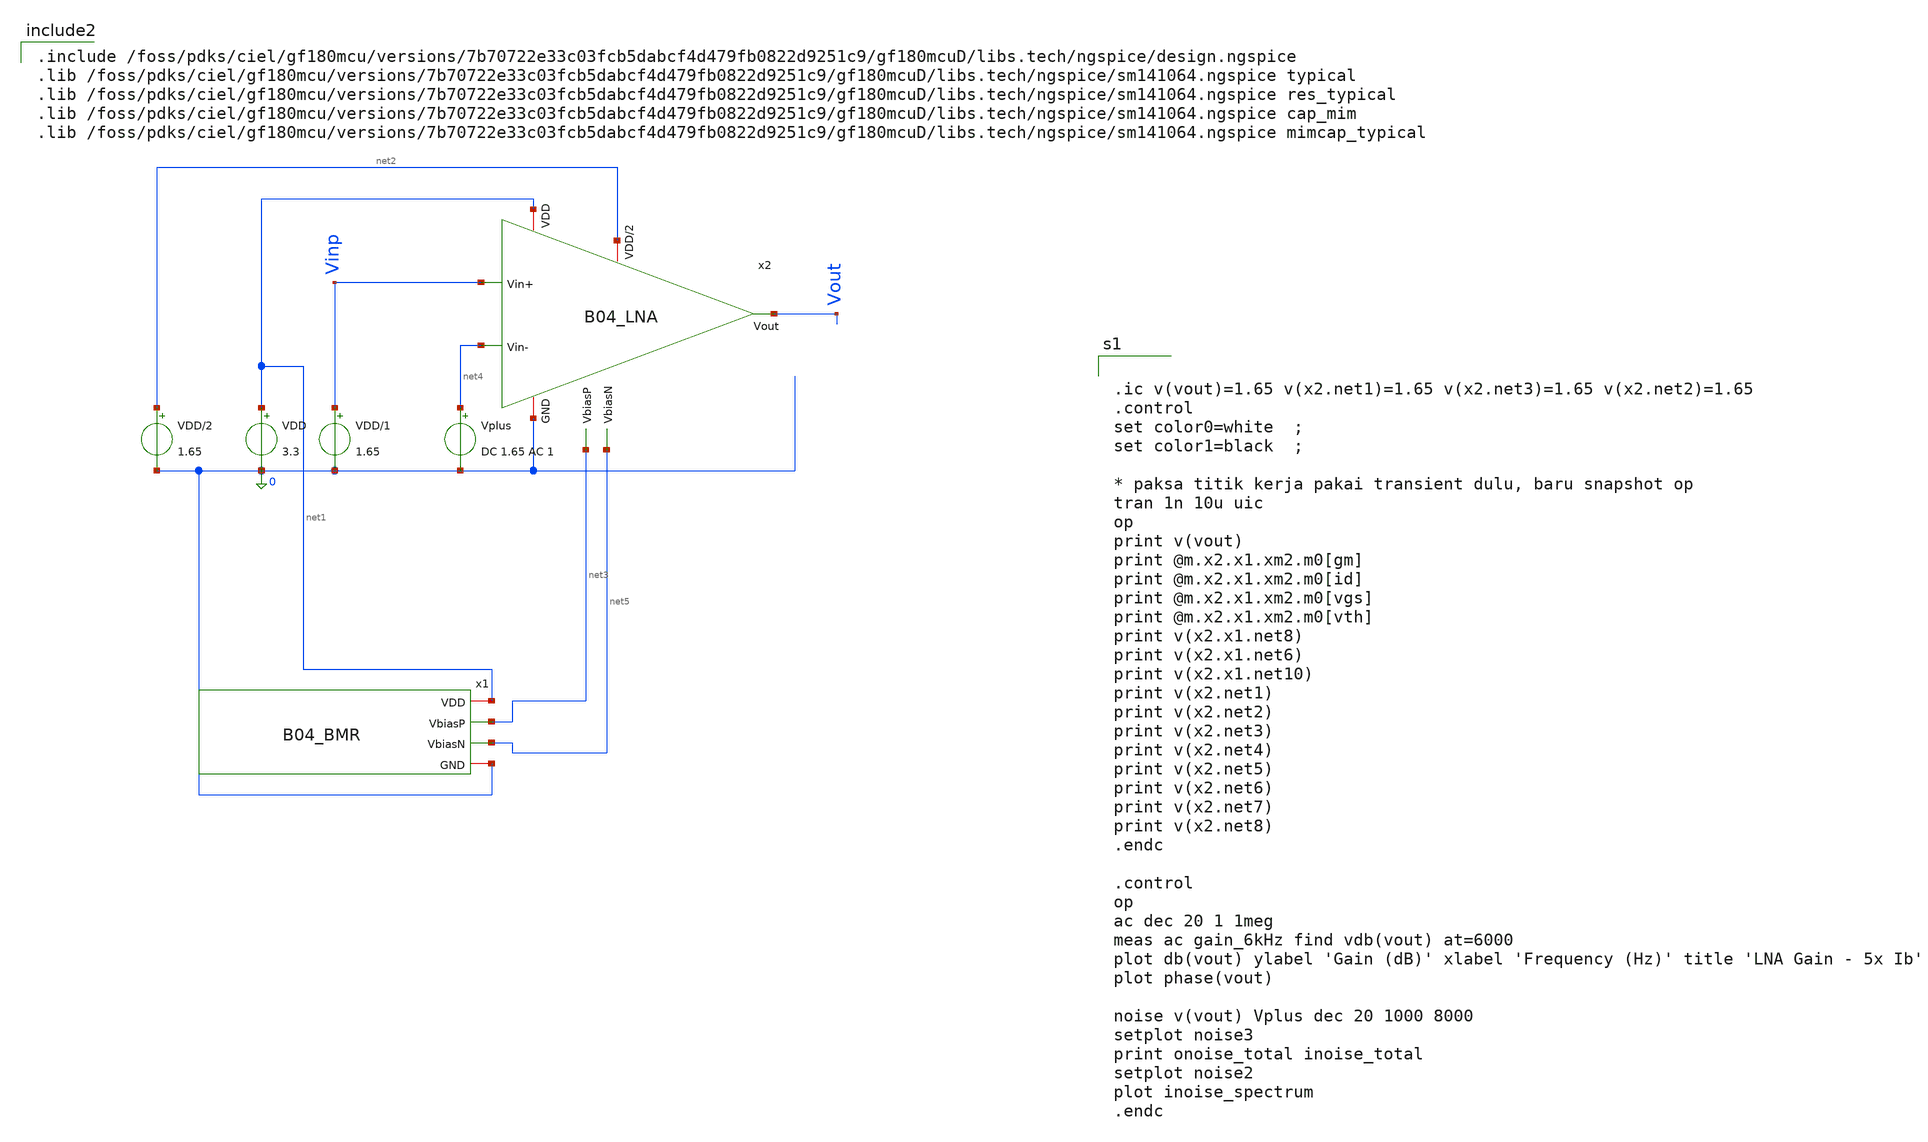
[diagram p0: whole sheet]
** sch_path: analog/B04_tb_LNA.sch
**.subckt B04_tb_LNA
VDD net1 0 3.3
Vplus net4 0 DC 1.65 AC 1
x2 net1 net2 Vinp Vout net4 0 net3 net5 B04_LNA
VDD/2 net2 0 1.65
VDD/1 Vinp 0 1.65
x1 net1 net3 net5 0 B04_BMR
**** begin user architecture code


.ic v(vout)=1.65 v(x2.net1)=1.65 v(x2.net3)=1.65 v(x2.net2)=1.65
.control
set color0=white  ;
set color1=black  ;

* paksa titik kerja pakai transient dulu, baru snapshot op
tran 1n 10u uic
op
print v(vout)
print @m.x2.x1.xm2.m0[gm]
print @m.x2.x1.xm2.m0[id]
print @m.x2.x1.xm2.m0[vgs]
print @m.x2.x1.xm2.m0[vth]
print v(x2.x1.net8)
print v(x2.x1.net6)
print v(x2.x1.net10)
print v(x2.net1)
print v(x2.net2)
print v(x2.net3)
print v(x2.net4)
print v(x2.net5)
print v(x2.net6)
print v(x2.net7)
print v(x2.net8)
.endc

.control
op
ac dec 20 1 1meg
meas ac gain_6kHz find vdb(vout) at=6000
plot db(vout) ylabel 'Gain (dB)' xlabel 'Frequency (Hz)' title 'LNA Gain - 5x Ib'
plot phase(vout)

noise v(vout) Vplus dec 20 1000 8000
setplot noise3
print onoise_total inoise_total
setplot noise2
plot inoise_spectrum
.endc



.include /foss/pdks/ciel/gf180mcu/versions/7b70722e33c03fcb5dabcf4d479fb0822d9251c9/gf180mcuD/libs.tech/ngspice/design.ngspice
.lib /foss/pdks/ciel/gf180mcu/versions/7b70722e33c03fcb5dabcf4d479fb0822d9251c9/gf180mcuD/libs.tech/ngspice/sm141064.ngspice typical
.lib /foss/pdks/ciel/gf180mcu/versions/7b70722e33c03fcb5dabcf4d479fb0822d9251c9/gf180mcuD/libs.tech/ngspice/sm141064.ngspice res_typical
.lib /foss/pdks/ciel/gf180mcu/versions/7b70722e33c03fcb5dabcf4d479fb0822d9251c9/gf180mcuD/libs.tech/ngspice/sm141064.ngspice cap_mim
.lib /foss/pdks/ciel/gf180mcu/versions/7b70722e33c03fcb5dabcf4d479fb0822d9251c9/gf180mcuD/libs.tech/ngspice/sm141064.ngspice mimcap_typical

**** end user architecture code
**.ends
.end
